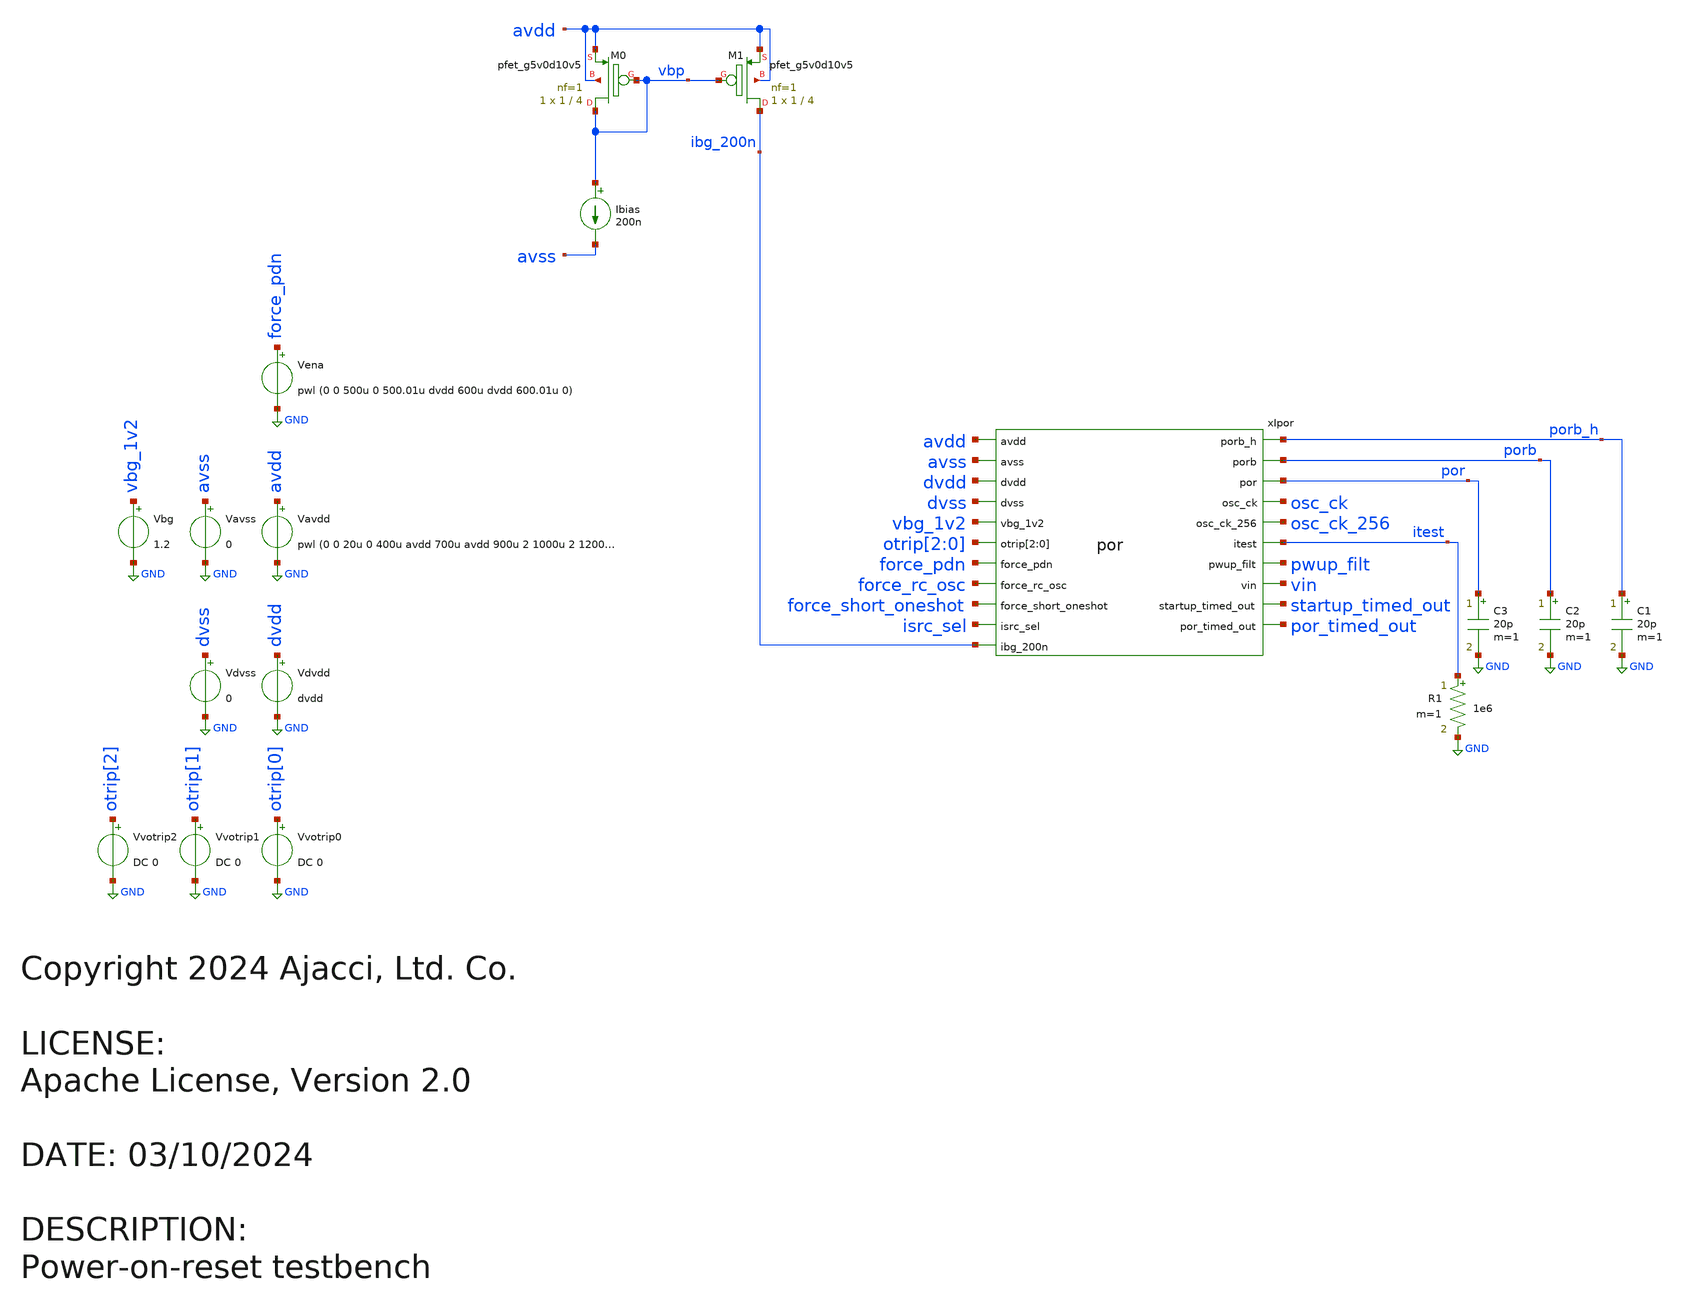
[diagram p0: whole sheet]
** sch_path: xschem/tb_por.sch
* Copyright 2024 Ajacci, Ltd. Co.
* LICENSE:
* Apache License, Version 2.0
**.subckt tb_por
Vavss avss GND 0
Vena force_pdn GND pwl (0 0 500u 0 500.01u dvdd 600u dvdd 600.01u 0)
Vavdd avdd GND pwl (0 0 20u 0 400u avdd 700u avdd 900u 2 1000u 2 1200u avdd)
.save i(vavdd)
Vbg vbg_1v2 GND 1.2
Ibias vbp avss 200n
XM1 ibg_200n vbp avdd avdd sky130_fd_pr__pfet_g5v0d10v5 L=4 W=1 nf=1 ad='int((nf+1)/2) * W/nf * 0.29'
+ as='int((nf+2)/2) * W/nf * 0.29' pd='2*int((nf+1)/2) * (W/nf + 0.29)' ps='2*int((nf+2)/2) * (W/nf + 0.29)'
+ nrd='0.29 / W' nrs='0.29 / W' sa=0 sb=0 sd=0 mult=1 m=1
XM0 vbp vbp avdd avdd sky130_fd_pr__pfet_g5v0d10v5 L=4 W=1 nf=1 ad='int((nf+1)/2) * W/nf * 0.29' as='int((nf+2)/2) * W/nf * 0.29'
+ pd='2*int((nf+1)/2) * (W/nf + 0.29)' ps='2*int((nf+2)/2) * (W/nf + 0.29)' nrd='0.29 / W' nrs='0.29 / W'
+ sa=0 sb=0 sd=0 mult=1 m=1
Vdvss dvss GND 0
Vdvdd dvdd GND dvdd
.save i(vdvdd)
R1 itest GND 1e6 m=1
C1 porb_h GND 20p m=1
C2 porb GND 20p m=1
C3 por GND 20p m=1
xIpor porb_h avdd avss porb dvdd por dvss osc_ck vbg_1v2 osc_ck_256 otrip[2] otrip[1] otrip[0] itest
+ pwup_filt force_pdn vin force_rc_osc force_short_oneshot startup_timed_out por_timed_out isrc_sel ibg_200n
+ por
Vvotrip0 otrip[0] GND DC 0
.save i(vvotrip0)
Vvotrip1 otrip[1] GND DC 0
.save i(vvotrip1)
Vvotrip2 otrip[2] GND DC 0
.save i(vvotrip2)
**** begin user architecture code


.param avdd=3.3
.param dvdd=1.8

.lib libs.tech/ngspice/sky130.lib.spice tt
.include libs.ref/sky130_fd_sc_hvl/spice/sky130_fd_sc_hvl.spice
.include libs.ref/sky130_fd_sc_hd/spice/sky130_fd_sc_hd.spice

*dig pull up/down to set test bits
R000 force_pdn dvss 1e9
R001 force_rc_osc dvss 1e9
R002 force_short_oneshot dvdd 1e9
R003 isrc_sel dvss 1e9

.temp 25
.save all
.save @m.xipor.xiana.xirsmux.xmena.msky130_fd_pr__nfet_g5v0d10v5[id]

.control
tran 10u 1400u
plot pwup_filt itest avdd force_pdn vbg_1v2 vin xipor.xiana.dcomp xipor.xiana.dcomp_filt
plot i(Vavdd) i(Vdvdd)
plot porb avdd pwup_filt*0.5
plot @m.xipor.xiana.xirsmux.xmena.msky130_fd_pr__nfet_g5v0d10v5[id]

.endc


**** end user architecture code
**.ends
.GLOBAL GND
.end
